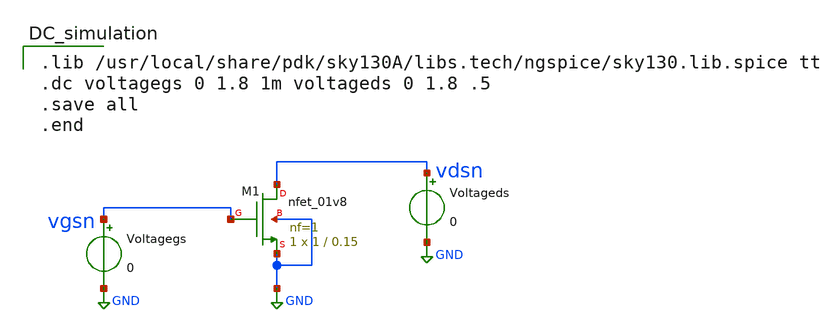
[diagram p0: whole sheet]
** sch_path: Xshem_files/dc_sweep.sch
**.subckt dc_sweep
XM1 vdsn vgsn GND GND sky130_fd_pr__nfet_01v8 L=0.15 W=1 nf=1 ad='int((nf+1)/2) * W/nf * 0.29' as='int((nf+2)/2) * W/nf * 0.29'
+ pd='2*int((nf+1)/2) * (W/nf + 0.29)' ps='2*int((nf+2)/2) * (W/nf + 0.29)' nrd='0.29 / W' nrs='0.29 / W'
+ sa=0 sb=0 sd=0 mult=1 m=1
Voltagegs vgsn GND 0
Voltageds vdsn GND 0
**** begin user architecture code

.lib /usr/local/share/pdk/sky130A/libs.tech/ngspice/sky130.lib.spice tt
.dc voltagegs 0 1.8 1m voltageds 0 1.8 .5
.save all
.end

**** end user architecture code
**.ends
.GLOBAL GND
.end
